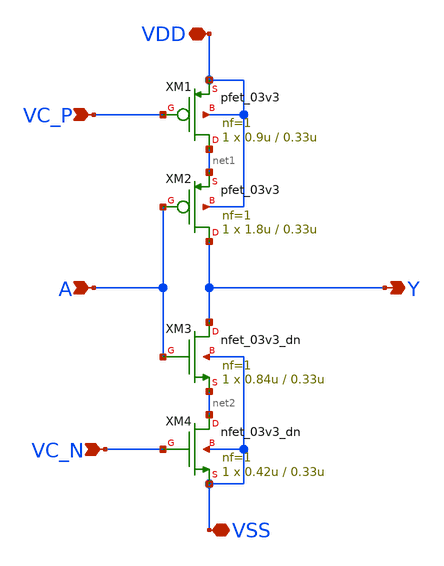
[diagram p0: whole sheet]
** sch_path: vco_inverter.sch
**.subckt vco_inverter VDD VSS A VC_N VC_P Y
*.iopin VDD
*.iopin VSS
*.ipin A
*.ipin VC_N
*.ipin VC_P
*.opin Y
XM1 net1 VC_P VDD VDD pfet_03v3 L=0.33u W=0.9u nf=1 ad='int((nf+1)/2) * W/nf * 0.18u' as='int((nf+2)/2) * W/nf * 0.18u'
+ pd='2*int((nf+1)/2) * (W/nf + 0.18u)' ps='2*int((nf+2)/2) * (W/nf + 0.18u)' nrd='0.18u / W' nrs='0.18u / W'
+ sa=0 sb=0 sd=0 m=1
XM2 Y A net1 VDD pfet_03v3 L=0.33u W=1.8u nf=1 ad='int((nf+1)/2) * W/nf * 0.18u' as='int((nf+2)/2) * W/nf * 0.18u'
+ pd='2*int((nf+1)/2) * (W/nf + 0.18u)' ps='2*int((nf+2)/2) * (W/nf + 0.18u)' nrd='0.18u / W' nrs='0.18u / W'
+ sa=0 sb=0 sd=0 m=1
XM3 Y A net2 VSS nfet_03v3_dn L=0.33u W=0.84u nf=1 ad='int((nf+1)/2) * W/nf * 0.18u' as='int((nf+2)/2) * W/nf * 0.18u'
+ pd='2*int((nf+1)/2) * (W/nf + 0.18u)' ps='2*int((nf+2)/2) * (W/nf + 0.18u)' nrd='0.18u / W' nrs='0.18u / W'
+ sa=0 sb=0 sd=0 m=1
XM4 net2 VC_N VSS VSS nfet_03v3_dn L=0.33u W=0.42u nf=1 ad='int((nf+1)/2) * W/nf * 0.18u' as='int((nf+2)/2) * W/nf * 0.18u'
+ pd='2*int((nf+1)/2) * (W/nf + 0.18u)' ps='2*int((nf+2)/2) * (W/nf + 0.18u)' nrd='0.18u / W' nrs='0.18u / W'
+ sa=0 sb=0 sd=0 m=1
**.ends
.end
